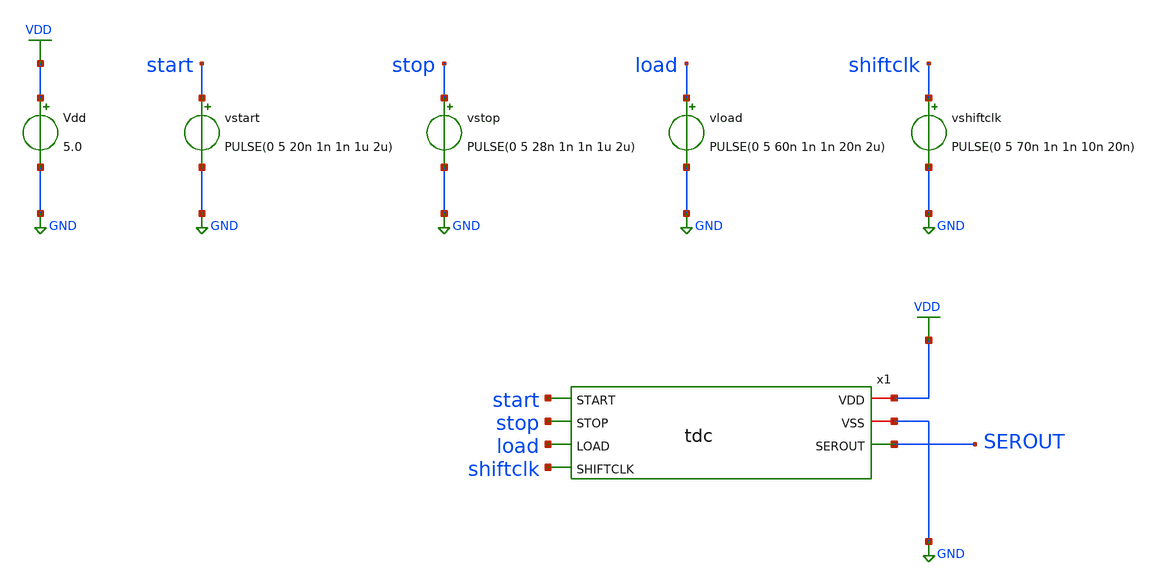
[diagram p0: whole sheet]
** sch_path: src/tdc_tb.sch
**.subckt tdc_tb
x1 VDD start stop GND load SEROUT shiftclk tdc
Vdd VDD GND 5.0
vstart start GND PULSE(0 5 20n 1n 1n 1u 2u)
vstop stop GND PULSE(0 5 28n 1n 1n 1u 2u)

vload load GND PULSE(0 5 60n 1n 1n 20n 2u)

vshiftclk shiftclk GND PULSE(0 5 70n 1n 1n 10n 20n)

**** begin user architecture code

.control

tran 50p 430n

* Measure actual START -> STOP interval
meas tran t_start WHEN v(START)=2.5 RISE=1
meas tran t_stop  WHEN v(STOP)=2.5 RISE=1
let t_delay = t_stop-t_start

echo ========================================
echo TDC FUNCTION TEST
echo ========================================
echo START crossing:
print t_start
echo STOP crossing:
print t_stop
echo START-to-STOP delay:
print t_delay

* First bit is already present on Q15 after parallel load.
* Sample halfway between SHIFTCLK rising edges.

meas tran b0  FIND v(SEROUT) AT=100n
meas tran b1  FIND v(SEROUT) AT=120n
meas tran b2  FIND v(SEROUT) AT=140n
meas tran b3  FIND v(SEROUT) AT=160n
meas tran b4  FIND v(SEROUT) AT=180n
meas tran b5  FIND v(SEROUT) AT=200n
meas tran b6  FIND v(SEROUT) AT=220n
meas tran b7  FIND v(SEROUT) AT=240n
meas tran b8  FIND v(SEROUT) AT=260n
meas tran b9  FIND v(SEROUT) AT=280n
meas tran b10 FIND v(SEROUT) AT=300n
meas tran b11 FIND v(SEROUT) AT=320n
meas tran b12 FIND v(SEROUT) AT=340n
meas tran b13 FIND v(SEROUT) AT=360n
meas tran b14 FIND v(SEROUT) AT=380n
meas tran b15 FIND v(SEROUT) AT=400n

let q0  = b0  > 2.5
let q1  = b1  > 2.5
let q2  = b2  > 2.5
let q3  = b3  > 2.5
let q4  = b4  > 2.5
let q5  = b5  > 2.5
let q6  = b6  > 2.5
let q7  = b7  > 2.5
let q8  = b8  > 2.5
let q9  = b9  > 2.5
let q10 = b10 > 2.5
let q11 = b11 > 2.5
let q12 = b12 > 2.5
let q13 = b13 > 2.5
let q14 = b14 > 2.5
let q15 = b15 > 2.5

echo ========================================
echo 16 SERIAL BITS:
print q0 q1 q2 q3 q4 q5 q6 q7
print q8 q9 q10 q11 q12 q13 q14 q15
echo ========================================

plot v(START) v(STOP) v(LOAD) v(SHIFTCLK) v(SEROUT)
plot v(x1.dly0) v(x1.dly1) v(x1.dly2) v(x1.dly3) v(x1.q0)+0.1 v(x1.q1)+0.2 v(x1.q2)+0.3 v(x1.q3)+0.4
+ v(x1.s0)-0.4 v(x1.s1)-0.3 v(x1.s2)-0.2 v(x1.s3)-0.1
.endc



 .include $::LIB/ip62_models
**** end user architecture code
**.ends
.GLOBAL VDD
.GLOBAL GND
.end
